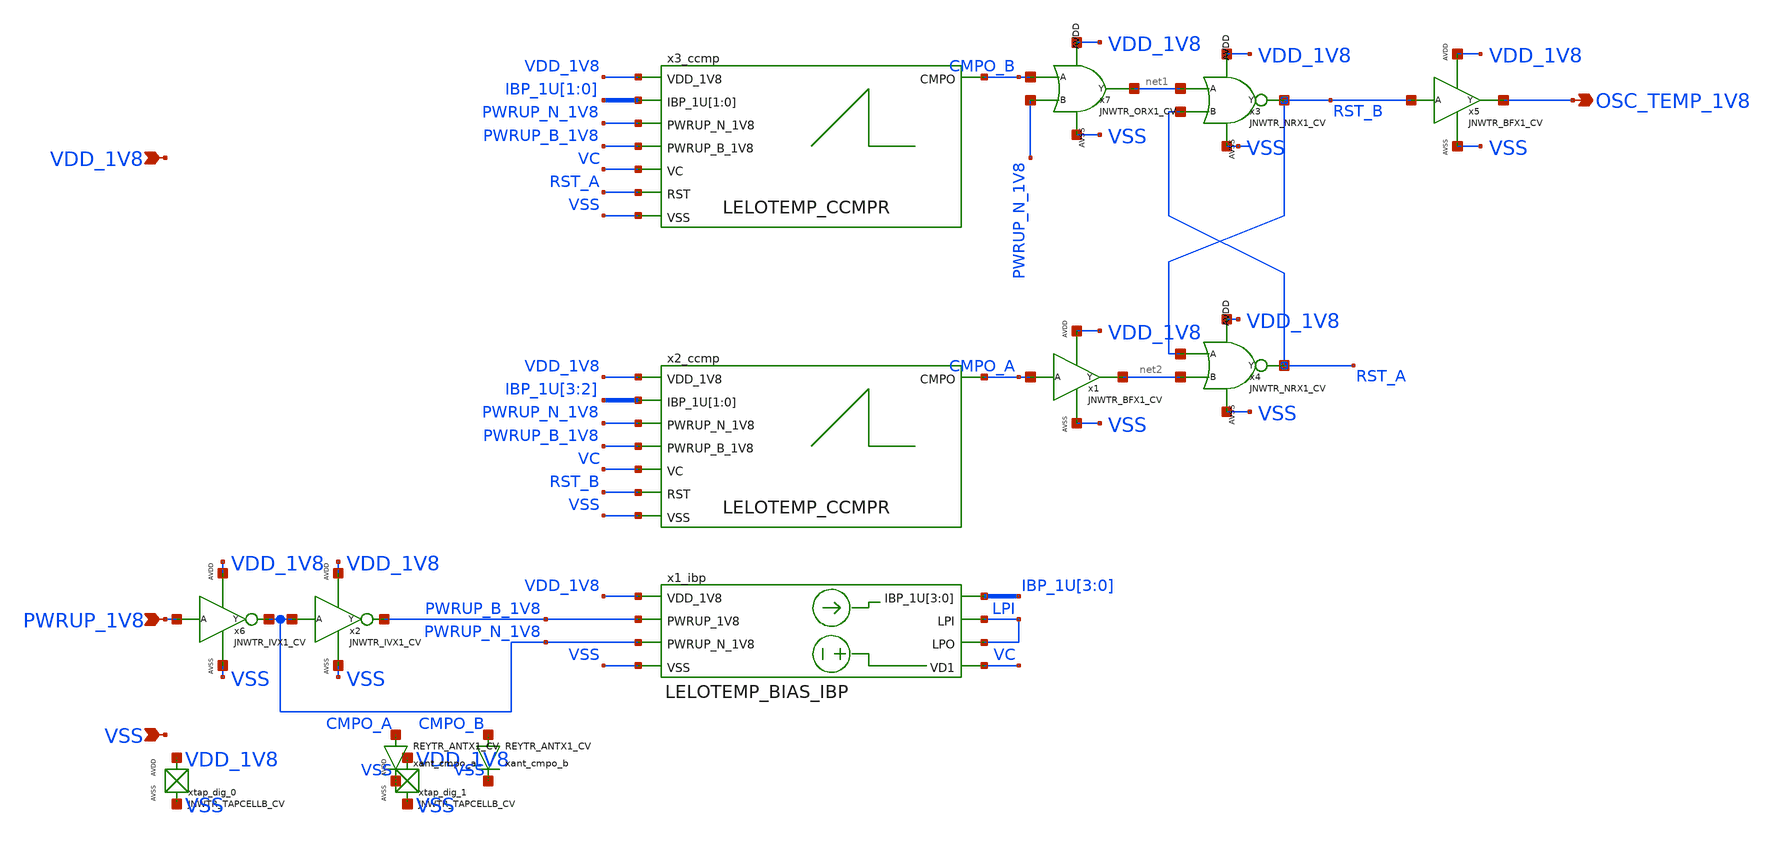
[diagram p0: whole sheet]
** sch_path: design/LELO_TEMP_SKY130A/LELO_TEMP.sch
**.subckt LELO_TEMP VDD_1V8 VSS PWRUP_1V8 OSC_TEMP_1V8
*.ipin VDD_1V8
*.ipin VSS
*.ipin PWRUP_1V8
*.opin OSC_TEMP_1V8
x1_ibp VDD_1V8 LPI IBP_1U[3] IBP_1U[2] IBP_1U[1] IBP_1U[0] LPI VC PWRUP_B_1V8 VSS PWRUP_N_1V8
+ LELOTEMP_BIAS_IBP
x6 PWRUP_1V8 PWRUP_N_1V8 VDD_1V8 VSS JNWTR_IVX1_CV
xtap_dig_0 VDD_1V8 VSS JNWTR_TAPCELLB_CV xoffset=0 yoffset=0 angle=0
xtap_dig_1 VDD_1V8 VSS JNWTR_TAPCELLB_CV xoffset=0 yoffset=0 angle=0
x2 PWRUP_N_1V8 PWRUP_B_1V8 VDD_1V8 VSS JNWTR_IVX1_CV
xant_cmpo_a CMPO_A VSS REYTR_ANTX1_CV
xant_cmpo_b CMPO_B VSS REYTR_ANTX1_CV
x3 net1 RST_A RST_B VDD_1V8 VSS JNWTR_NRX1_CV
x4 RST_B net2 RST_A VDD_1V8 VSS JNWTR_NRX1_CV
x7 CMPO_B PWRUP_N_1V8 net1 VDD_1V8 VSS JNWTR_ORX1_CV xoffset=0 yoffset=0 angle=0 M=1
x3_ccmp IBP_1U[1] IBP_1U[0] VDD_1V8 PWRUP_N_1V8 PWRUP_B_1V8 CMPO_B VC RST_A VSS LELOTEMP_CCMPR
x2_ccmp IBP_1U[3] IBP_1U[2] VDD_1V8 PWRUP_N_1V8 PWRUP_B_1V8 CMPO_A VC RST_B VSS LELOTEMP_CCMPR
**.ends
.end
